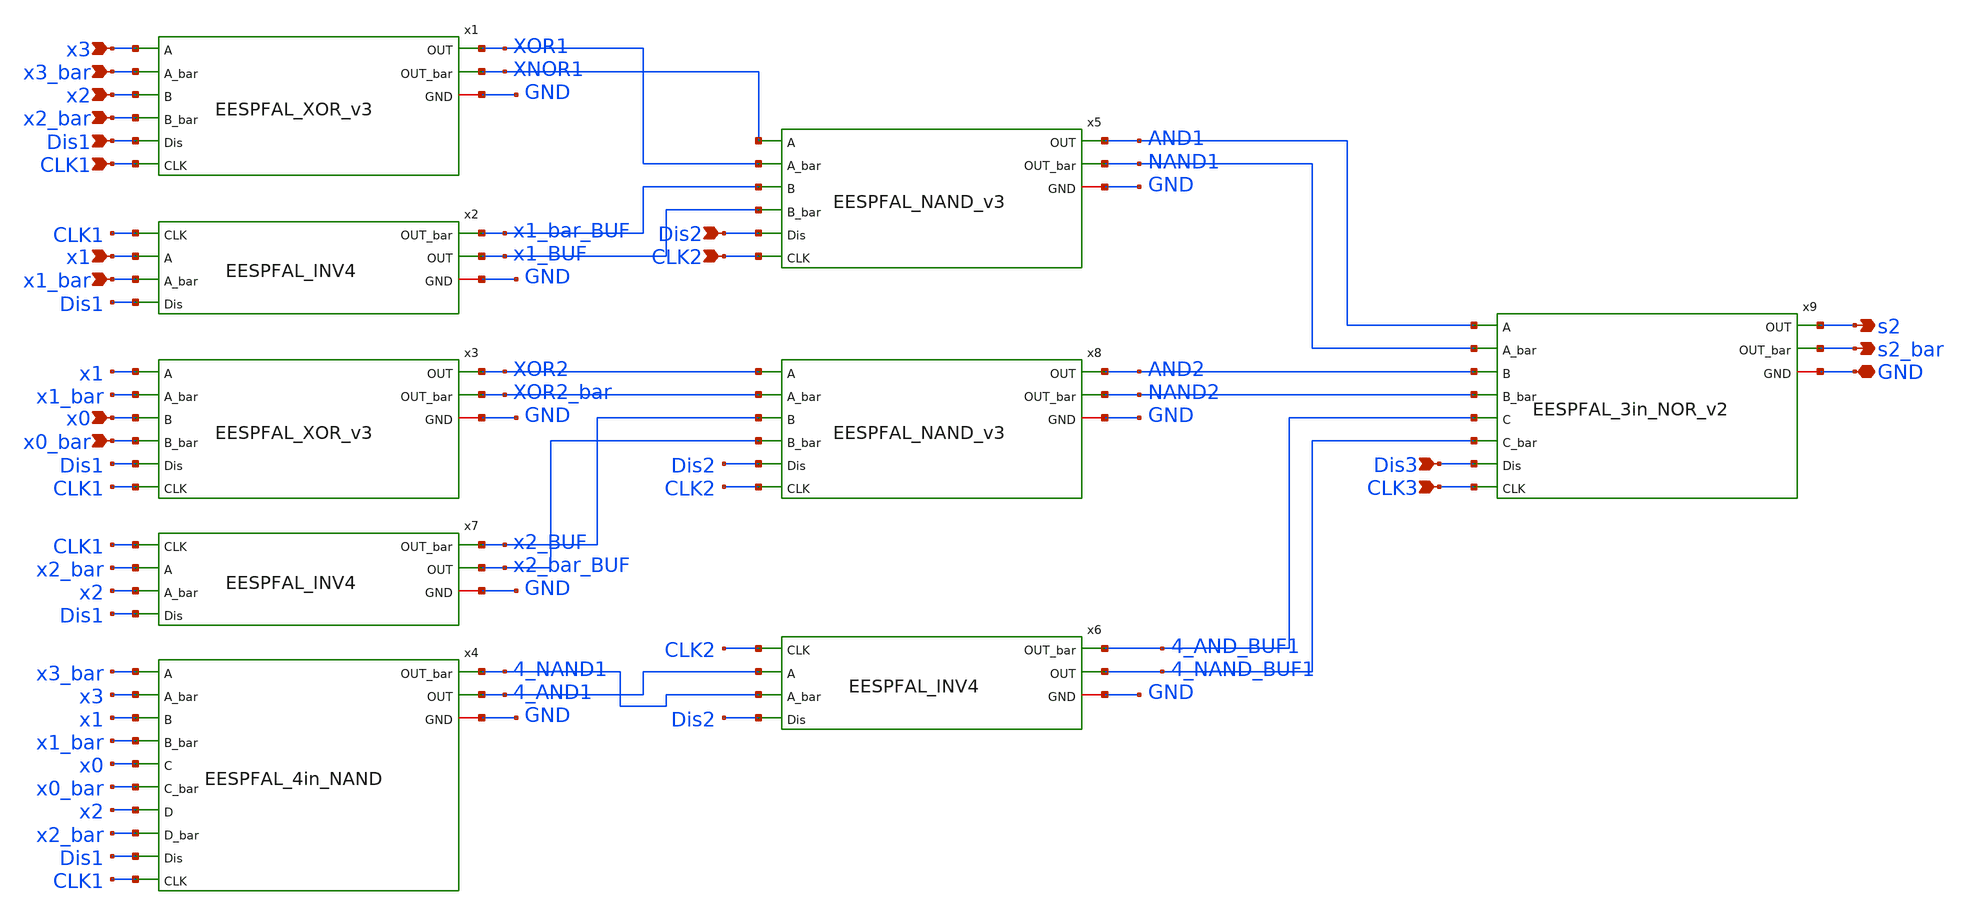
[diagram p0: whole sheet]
** sch_path: skywater_stuff/EESPFAL_s2_draft2.sch
**.subckt EESPFAL_s2_draft2 x0 x0_bar x1 x1_bar x2 x2_bar x3 x3_bar s2 s2_bar Dis1 Dis2 Dis3 GND
*+ CLK1 CLK2 CLK3
*.ipin x0
*.ipin x0_bar
*.ipin x1
*.ipin x1_bar
*.ipin x2
*.ipin x2_bar
*.ipin x3
*.ipin x3_bar
*.opin s2
*.opin s2_bar
*.ipin Dis1
*.ipin Dis2
*.ipin Dis3
*.iopin GND
*.ipin CLK1
*.ipin CLK2
*.ipin CLK3
x5 XNOR1 XOR1 x1_bar_BUF x1_BUF AND1 NAND1 Dis2 GND CLK2 EESPFAL_NAND_v3
x6 4_AND1 4_NAND1 4_NAND_BUF1 4_AND_BUF1 Dis2 GND CLK2 EESPFAL_INV4
x8 XOR2 XOR2_bar x2_BUF x2_bar_BUF AND2 NAND2 Dis2 GND CLK2 EESPFAL_NAND_v3
x9 AND1 NAND1 AND2 NAND2 4_AND_BUF1 4_NAND_BUF1 s2 s2_bar Dis3 GND CLK3 EESPFAL_3in_NOR_v2
x4 x3_bar x3 x1 x1_bar x0 x0_bar x2 x2_bar 4_AND1 4_NAND1 Dis1 GND CLK1 EESPFAL_4in_NAND
x1 x3 x3_bar x2 x2_bar XOR1 XNOR1 Dis1 GND CLK1 EESPFAL_XOR_v3
x2 x1 x1_bar x1_BUF x1_bar_BUF Dis1 GND CLK1 EESPFAL_INV4
x3 x1 x1_bar x0 x0_bar XOR2 XOR2_bar Dis1 GND CLK1 EESPFAL_XOR_v3
x7 x2_bar x2 x2_bar_BUF x2_BUF Dis1 GND CLK1 EESPFAL_INV4
**.ends
.end
